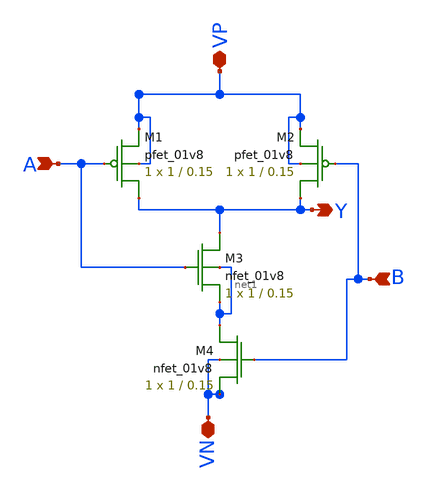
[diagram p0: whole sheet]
** sch_path: MiniProject1-AND/XSCHEM/NAND.sch
**.subckt NAND A VN Y VP B
*.ipin A
*.iopin VN
*.opin Y
*.iopin VP
*.ipin B
XM1 Y A VP VP sky130_fd_pr__pfet_01v8 L=0.15 W=1 nf=1 ad='int((nf+1)/2) * W/nf * 0.29' as='int((nf+2)/2) * W/nf * 0.29'
+ pd='2*int((nf+1)/2) * (W/nf + 0.29)' ps='2*int((nf+2)/2) * (W/nf + 0.29)' nrd='0.29 / W' nrs='0.29 / W'
+ sa=0 sb=0 sd=0 mult=1 m=1
XM2 Y B VP VP sky130_fd_pr__pfet_01v8 L=0.15 W=1 nf=1 ad='int((nf+1)/2) * W/nf * 0.29' as='int((nf+2)/2) * W/nf * 0.29'
+ pd='2*int((nf+1)/2) * (W/nf + 0.29)' ps='2*int((nf+2)/2) * (W/nf + 0.29)' nrd='0.29 / W' nrs='0.29 / W'
+ sa=0 sb=0 sd=0 mult=1 m=1
XM3 Y A net1 net1 sky130_fd_pr__nfet_01v8 L=0.15 W=1 nf=1 ad='int((nf+1)/2) * W/nf * 0.29' as='int((nf+2)/2) * W/nf * 0.29'
+ pd='2*int((nf+1)/2) * (W/nf + 0.29)' ps='2*int((nf+2)/2) * (W/nf + 0.29)' nrd='0.29 / W' nrs='0.29 / W'
+ sa=0 sb=0 sd=0 mult=1 m=1
XM4 net1 B VN VN sky130_fd_pr__nfet_01v8 L=0.15 W=1 nf=1 ad='int((nf+1)/2) * W/nf * 0.29' as='int((nf+2)/2) * W/nf * 0.29'
+ pd='2*int((nf+1)/2) * (W/nf + 0.29)' ps='2*int((nf+2)/2) * (W/nf + 0.29)' nrd='0.29 / W' nrs='0.29 / W'
+ sa=0 sb=0 sd=0 mult=1 m=1
**.ends
.end
